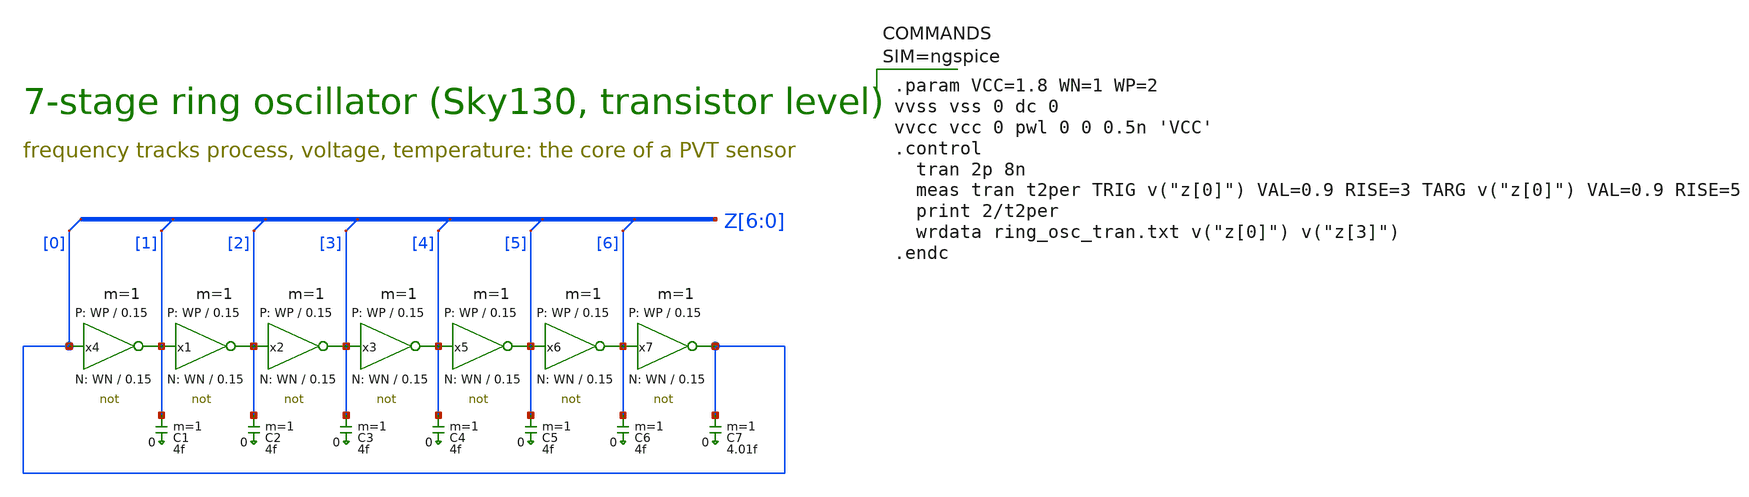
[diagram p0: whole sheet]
** sch_path: analog/ring_osc/ring_osc.sch
* (Copyright 2021 Stefan Frederik Schippers, Apache-2.0).
* StefanSchippers/xschem_sky130/sky130_tests/not.sch:
* Copyright 2021 Stefan Frederik Schippers
* Licensed under the Apache License, Version 2.0 (the "License");
**.subckt ring_osc
C1 Z[1] 0 4f m=1
C2 Z[2] 0 4f m=1
C3 Z[3] 0 4f m=1
C4 Z[4] 0 4f m=1
C5 Z[5] 0 4f m=1
C6 Z[6] 0 4f m=1
C7 Z[0] 0 4.01f m=1
x4 Z[1] Z[0] VCC VSS not W_N=WN L_N=0.15 W_P=WP L_P=0.15 m=1
x1 Z[2] Z[1] VCC VSS not W_N=WN L_N=0.15 W_P=WP L_P=0.15 m=1
x2 Z[3] Z[2] VCC VSS not W_N=WN L_N=0.15 W_P=WP L_P=0.15 m=1
x3 Z[4] Z[3] VCC VSS not W_N=WN L_N=0.15 W_P=WP L_P=0.15 m=1
x5 Z[5] Z[4] VCC VSS not W_N=WN L_N=0.15 W_P=WP L_P=0.15 m=1
x6 Z[6] Z[5] VCC VSS not W_N=WN L_N=0.15 W_P=WP L_P=0.15 m=1
x7 Z[0] Z[6] VCC VSS not W_N=WN L_N=0.15 W_P=WP L_P=0.15 m=1
* tap: Z[6:0] --> Z[0]
* tap: Z[6:0] --> Z[1]
* tap: Z[6:0] --> Z[2]
* tap: Z[6:0] --> Z[3]
* tap: Z[6:0] --> Z[4]
* tap: Z[6:0] --> Z[5]
* tap: Z[6:0] --> Z[6]
**** begin user architecture code


.param VCC=1.8 WN=1 WP=2
vvss vss 0 dc 0
vvcc vcc 0 pwl 0 0 0.5n 'VCC'
.control
  tran 2p 8n
  meas tran t2per TRIG v("z[0]") VAL=0.9 RISE=3 TARG v("z[0]") VAL=0.9 RISE=5
  print 2/t2per
  wrdata ring_osc_tran.txt v("z[0]") v("z[3]")
.endc




.lib $::SKYWATER_MODELS/sky130.lib.spice tt

**** end user architecture code
**.ends

* expanding   symbol:  sky130_tests/not.sym # of pins=2
** sym_path: sky130_tests/not.sym
** sch_path: sky130_tests/not.sch
.subckt not y a VCCPIN VSSPIN     W_N=1 L_N=0.15 W_P=2 L_P=0.15
*.opin y
*.ipin a
XM1 DN a VSSPIN VSSPIN sky130_fd_pr__nfet_01v8 L=L_N W=W_N nf=1 ad='int((1 + 1)/2) * W_N / 1 * 0.29'
+ as='int((1 + 2)/2) * W_N / 1 * 0.29' pd='2*int((1 + 1)/2) * (W_N / 1 + 0.29)' ps='2*int((1 + 2)/2) * (W_N / 1 + 0.29)'
+ nrd='0.29 / W_N ' nrs='0.29 / W_N ' sa=0 sb=0 sd=0 mult=1 m=1
XM2 DP a VCCPIN VCCPIN sky130_fd_pr__pfet_01v8 L=L_P W=W_P nf=1 ad='int((nf+1)/2) * W/nf * 0.29' as='int((nf+2)/2) * W/nf * 0.29'
+ pd='2*int((nf+1)/2) * (W/nf + 0.29)' ps='2*int((nf+2)/2) * (W/nf + 0.29)' nrd='0.29 / W' nrs='0.29 / W'
+ sa=0 sb=0 sd=0 mult=1 m=1
Vmeas DP y 0
.save i(vmeas)
Vmeas1 y DN 0
.save i(vmeas1)
.save v(dp)
.save v(dn)
.ends

.end
